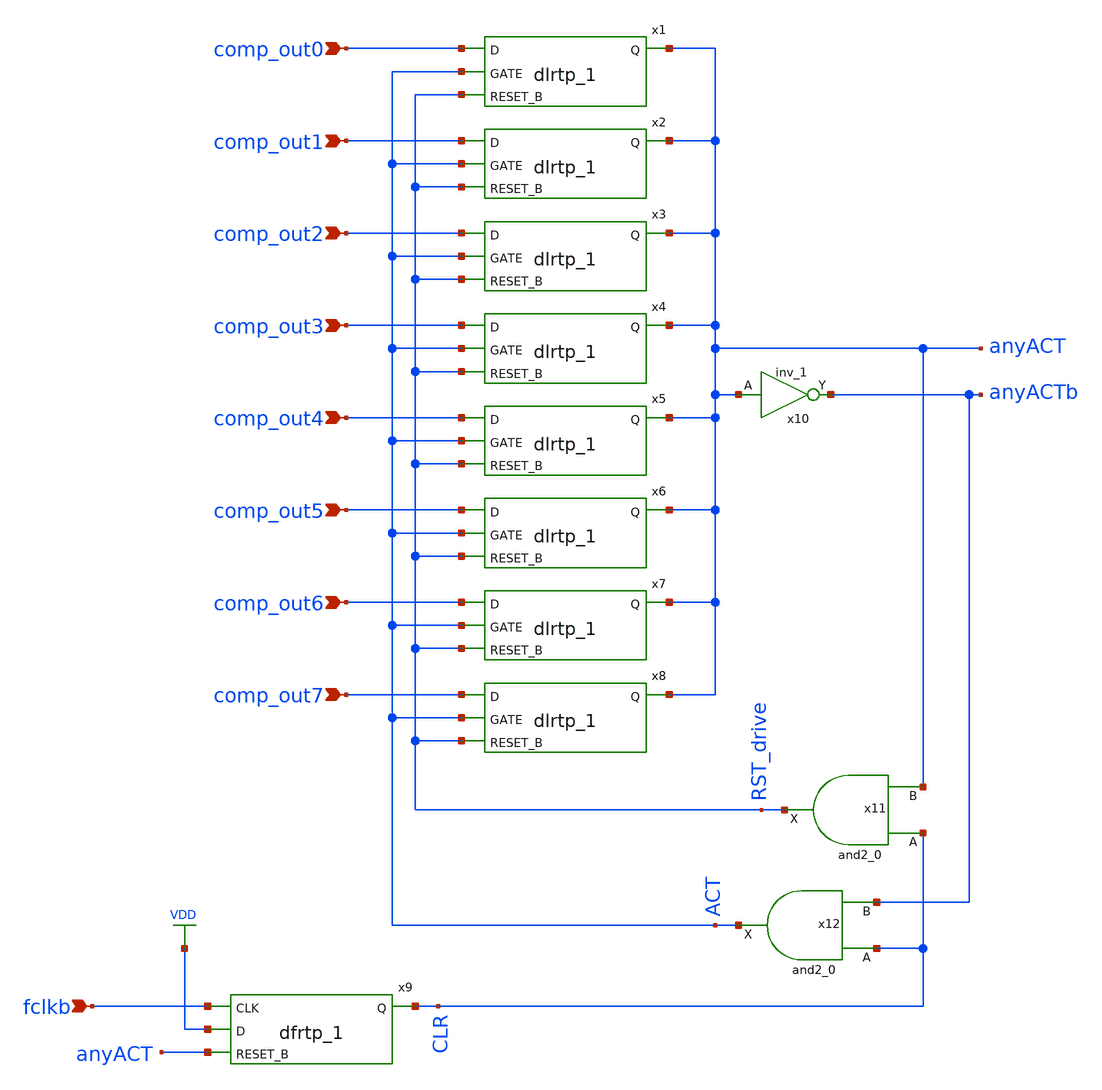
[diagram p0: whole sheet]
** sch_path: xschem/readout/CLR_ACT.sch
**.subckt CLR_ACT comp_out0 comp_out1 comp_out2 comp_out3 comp_out4 comp_out5 comp_out6 comp_out7
*+ fclkb
*.ipin comp_out0
*.ipin comp_out1
*.ipin comp_out2
*.ipin comp_out3
*.ipin comp_out4
*.ipin comp_out5
*.ipin comp_out6
*.ipin comp_out7
*.ipin fclkb
x1 comp_out0 ACT RST_drive VGND VNB VPB VPWR anyACT sky130_fd_sc_hd__dlrtp_1
x2 comp_out1 ACT RST_drive VGND VNB VPB VPWR anyACT sky130_fd_sc_hd__dlrtp_1
x3 comp_out2 ACT RST_drive VGND VNB VPB VPWR anyACT sky130_fd_sc_hd__dlrtp_1
x4 comp_out3 ACT RST_drive VGND VNB VPB VPWR anyACT sky130_fd_sc_hd__dlrtp_1
x5 comp_out4 ACT RST_drive VGND VNB VPB VPWR anyACT sky130_fd_sc_hd__dlrtp_1
x6 comp_out5 ACT RST_drive VGND VNB VPB VPWR anyACT sky130_fd_sc_hd__dlrtp_1
x7 comp_out6 ACT RST_drive VGND VNB VPB VPWR anyACT sky130_fd_sc_hd__dlrtp_1
x8 comp_out7 ACT RST_drive VGND VNB VPB VPWR anyACT sky130_fd_sc_hd__dlrtp_1
x9 fclkb VDD anyACT VGND VNB VPB VPWR CLR sky130_fd_sc_hd__dfrtp_1
x10 anyACT VGND VNB VPB VPWR anyACTb sky130_fd_sc_hd__inv_1
x11 CLR anyACT VGND VNB VPB VPWR RST_drive sky130_fd_sc_hd__and2_0
x12 CLR anyACTb VGND VNB VPB VPWR ACT sky130_fd_sc_hd__and2_0
**.ends
.GLOBAL VDD
.end
